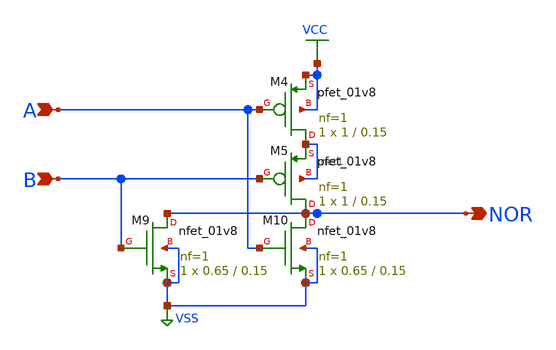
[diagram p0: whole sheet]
** sch_path: blocks/rom/rom_nor2.sch
**.subckt rom_nor2 A NOR B
*.ipin A
*.opin NOR
*.ipin B
XM4 net1 A VCC VCC sky130_fd_pr__pfet_01v8 L=0.15 W=1 nf=1 ad='int((nf+1)/2) * W/nf * 0.29' as='int((nf+2)/2) * W/nf * 0.29'
+ pd='2*int((nf+1)/2) * (W/nf + 0.29)' ps='2*int((nf+2)/2) * (W/nf + 0.29)' nrd='0.29 / W' nrs='0.29 / W'
+ sa=0 sb=0 sd=0 mult=1 m=1
XM5 NOR B net1 net1 sky130_fd_pr__pfet_01v8 L=0.15 W=1 nf=1 ad='int((nf+1)/2) * W/nf * 0.29' as='int((nf+2)/2) * W/nf * 0.29'
+ pd='2*int((nf+1)/2) * (W/nf + 0.29)' ps='2*int((nf+2)/2) * (W/nf + 0.29)' nrd='0.29 / W' nrs='0.29 / W'
+ sa=0 sb=0 sd=0 mult=1 m=1
XM9 NOR B VSS VSS sky130_fd_pr__nfet_01v8 L=0.15 W=0.65 nf=1 ad='int((1 + 1)/2) * 0.65 / 1 * 0.29' as='int((1 + 2)/2) * 0.65 / 1 * 0.29'
+ pd='2*int((1 + 1)/2) * (0.65 / 1 + 0.29)' ps='2*int((1 + 2)/2) * (0.65 / 1 + 0.29)' nrd='0.29 / 0.65 '
+ nrs='0.29 / 0.65 ' sa=0 sb=0 sd=0 mult=1 m=1
XM10 NOR A VSS VSS sky130_fd_pr__nfet_01v8 L=0.15 W=0.65 nf=1 ad='int((1 + 1)/2) * 0.65 / 1 * 0.29' as='int((1 + 2)/2) * 0.65 / 1 * 0.29'
+ pd='2*int((1 + 1)/2) * (0.65 / 1 + 0.29)' ps='2*int((1 + 2)/2) * (0.65 / 1 + 0.29)' nrd='0.29 / 0.65 '
+ nrs='0.29 / 0.65 ' sa=0 sb=0 sd=0 mult=1 m=1
**.ends
.GLOBAL VCC
.GLOBAL VSS
.end
